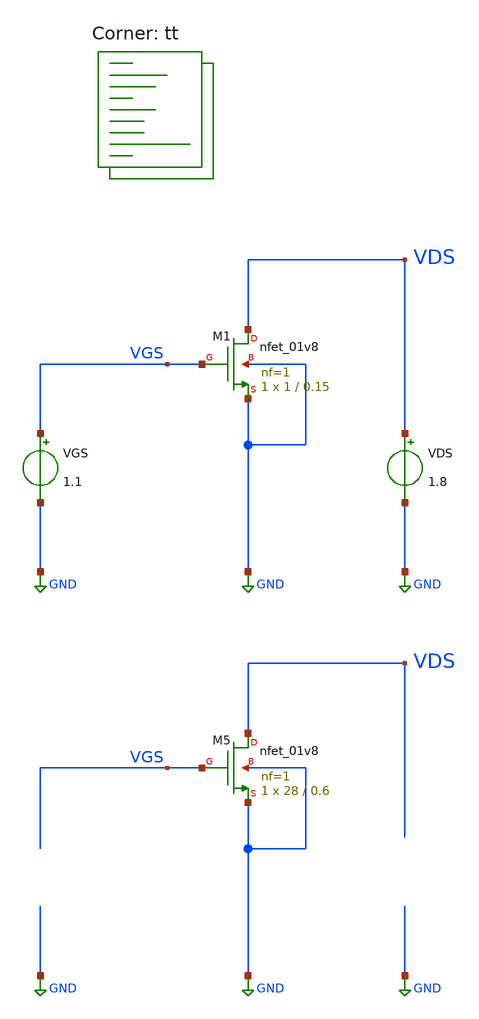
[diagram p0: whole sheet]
** sch_path: projects/opamp/xschem_ngspice/vds_vgs_sweep_nfet_2.sch
**.subckt vds_vgs_sweep_nfet_2
XM1 VDS VGS GND GND sky130_fd_pr__nfet_01v8 L=0.15 W=1 nf=1 ad='int((nf+1)/2) * W/nf * 0.29' as='int((nf+2)/2) * W/nf * 0.29'
+ pd='2*int((nf+1)/2) * (W/nf + 0.29)' ps='2*int((nf+2)/2) * (W/nf + 0.29)' nrd='0.29 / W' nrs='0.29 / W'
+ sa=0 sb=0 sd=0 mult=1 m=1
VGS VGS GND 1.1
VDS VDS GND 1.8
XM5 VDS VGS GND GND sky130_fd_pr__nfet_01v8 L=0.6 W=28 nf=1 ad='int((nf+1)/2) * W/nf * 0.29' as='int((nf+2)/2) * W/nf * 0.29'
+ pd='2*int((nf+1)/2) * (W/nf + 0.29)' ps='2*int((nf+2)/2) * (W/nf + 0.29)' nrd='0.29 / W' nrs='0.29 / W'
+ sa=0 sb=0 sd=0 mult=1 m=1
**** begin user architecture code
.lib $::SKYWATER_MODELS/sky130.lib.spice tt



.option method=gear
.option wnflag=1
.option savecurrents

.save @m.xm1.msky130_fd_pr__nfet_01v8[gm] @m.xm1.msky130_fd_pr__nfet_01v8[gds] @m.xm1.msky130_fd_pr__nfet_01v8[vth] @m.xm2.msky130_fd_pr__nfet_01v8[gm] @m.xm2.msky130_fd_pr__nfet_01v8[gds] @m.xm2.msky130_fd_pr__nfet_01v8[vth] @m.xm3.msky130_fd_pr__nfet_01v8[gm] @m.xm3.msky130_fd_pr__nfet_01v8[gds] @m.xm3.msky130_fd_pr__nfet_01v8[vth] @m.xm4.msky130_fd_pr__nfet_01v8[gm] @m.xm4.msky130_fd_pr__nfet_01v8[gds] @m.xm5.msky130_fd_pr__nfet_01v8[gm] @m.xm5.msky130_fd_pr__nfet_01v8[gds] @m.xm6.msky130_fd_pr__nfet_01v8[gm] @m.xm6.msky130_fd_pr__nfet_01v8[gds] @m.xm7.msky130_fd_pr__nfet_01v8[gm] @m.xm7.msky130_fd_pr__nfet_01v8[gds] @m.xm8.msky130_fd_pr__nfet_01v8[gm] @m.xm8.msky130_fd_pr__nfet_01v8[gds] @m.xm9.msky130_fd_pr__nfet_01v8[gm] @m.xm9.msky130_fd_pr__nfet_01v8[gds] @m.xm10.msky130_fd_pr__nfet_01v8[gm] @m.xm10.msky130_fd_pr__nfet_01v8[gds]


.control
  save all
  * dc VGS 0 1.8 0.001 VDS 0 1.8 0.1
  dc VDS 0.0 0.9 0.001 VGS 0.7 1.1 0.01
  remzerovec
  write vds_vgs_sweep_nfet_2.raw
  set appendwrite
  show
.endc



**** end user architecture code
**.ends
.GLOBAL GND
.end
